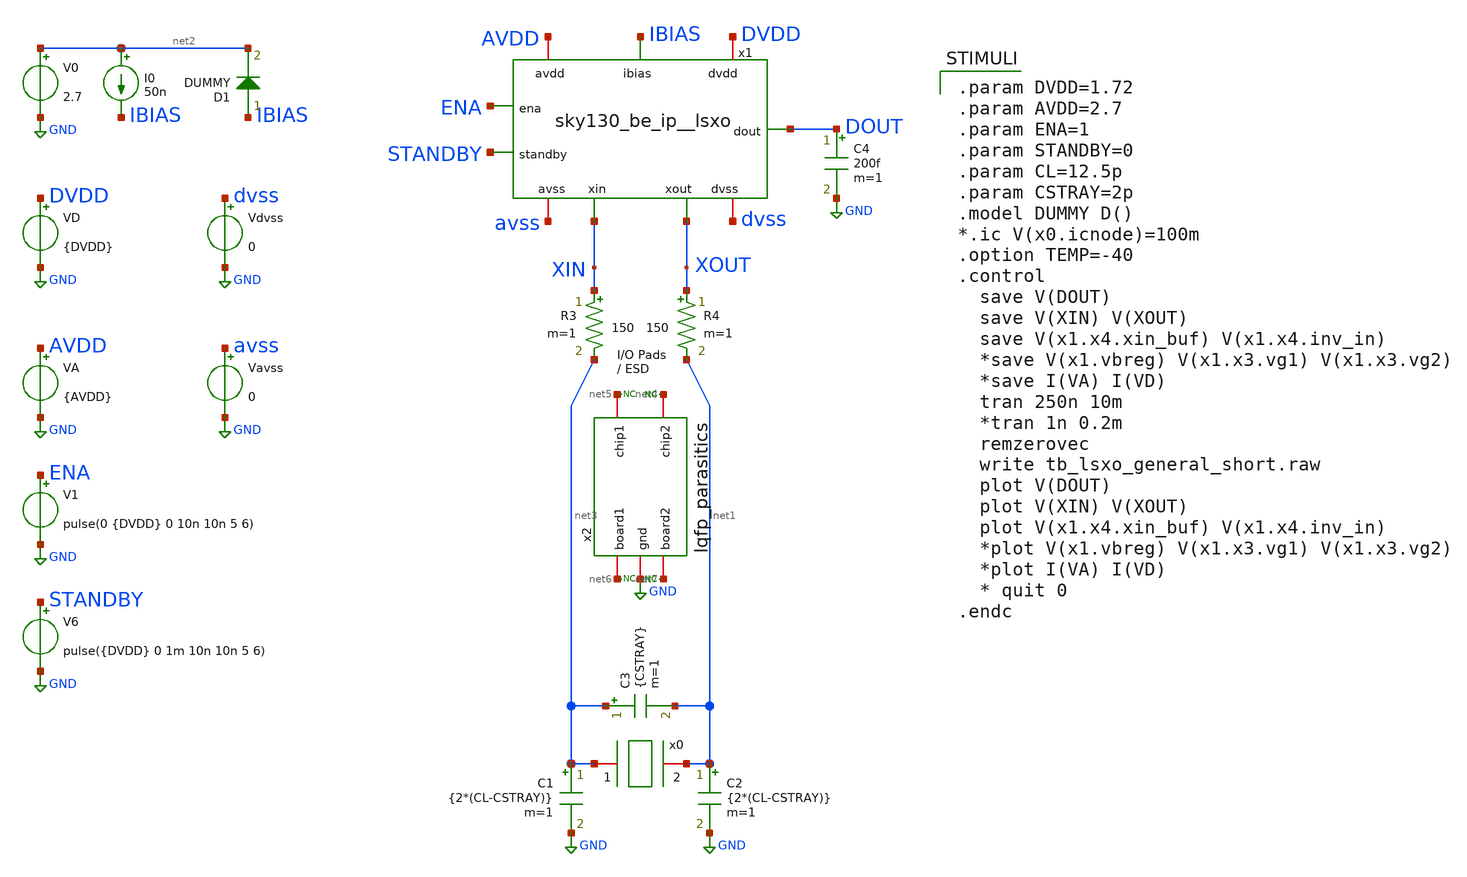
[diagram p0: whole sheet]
** sch_path: xschem/tb_man__sky130_be_ip__lsxo.sch

.lib $::SKYWATER_MODELS/sky130.lib.spice fs
.include $::SKYWATER_STDCELLS/sky130_fd_sc_hd.spice

**.subckt tb_man__sky130_be_ip__lsxo
VD DVDD GND {DVDD}
VA AVDD GND {AVDD}
C1 net3 GND {2*(CL-CSTRAY)} m=1
C2 net1 GND {2*(CL-CSTRAY)} m=1
C3 net3 net1 {CSTRAY} m=1
I0 net2 IBIAS 50n
C4 DOUT GND 200f m=1
V0 net2 GND 2.7
V6 STANDBY GND pulse({DVDD} 0 1m 10n 10n 5 6)
R3 XIN net3 150 m=1
R4 XOUT net1 150 m=1
x2 net4 net5 GND net6 net7 lqfp_parasitics
V1 ENA GND pulse(0 {DVDD} 0 10n 10n 5 6)
D1 IBIAS net2 DUMMY area=100
x1 AVDD avss DVDD dvss IBIAS ENA STANDBY DOUT XIN XOUT sky130_be_ip__lsxo
x0 net3 net1 xtal_iqd_125_1
Vdvss dvss GND 0
Vavss avss GND 0
* noconn #net4
* noconn #net7
* noconn #net6
* noconn #net5
**** begin user architecture code

.param DVDD=1.72
.param AVDD=2.7
.param ENA=1
.param STANDBY=0
.param CL=12.5p
.param CSTRAY=2p
.model DUMMY D()
*.ic V(x0.icnode)=100m
.option TEMP=-40
.control
  save V(DOUT)
  save V(XIN) V(XOUT)
  save V(x1.x4.xin_buf) V(x1.x4.inv_in)
  *save V(x1.vbreg) V(x1.x3.vg1) V(x1.x3.vg2)
  *save I(VA) I(VD)
  tran 250n 10m
  *tran 1n 0.2m
  remzerovec
  write tb_lsxo_general_short.raw
  plot V(DOUT)
  plot V(XIN) V(XOUT)
  plot V(x1.x4.xin_buf) V(x1.x4.inv_in)
  *plot V(x1.vbreg) V(x1.x3.vg1) V(x1.x3.vg2)
  *plot I(VA) I(VD)
  * quit 0
.endc

**** end user architecture code
**.ends
.GLOBAL GND
.end
